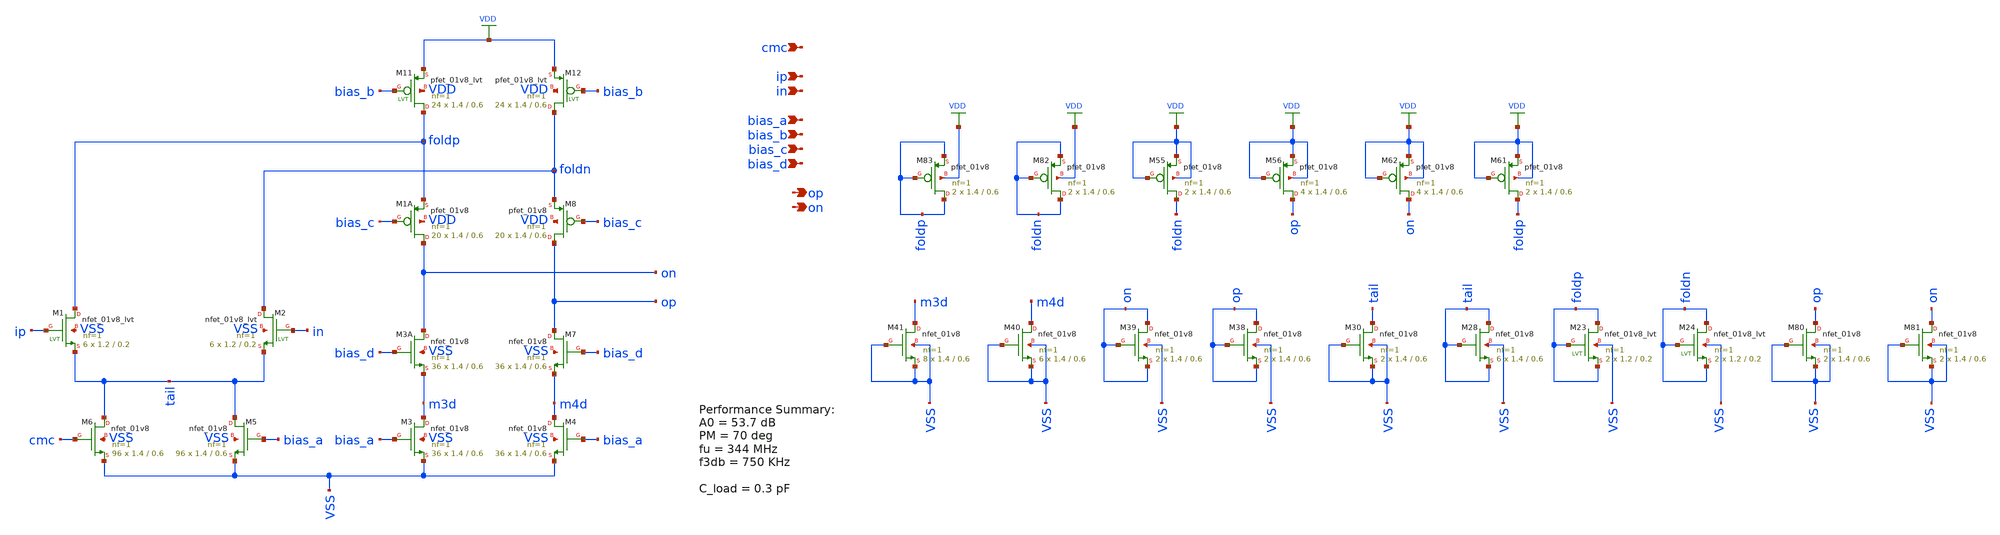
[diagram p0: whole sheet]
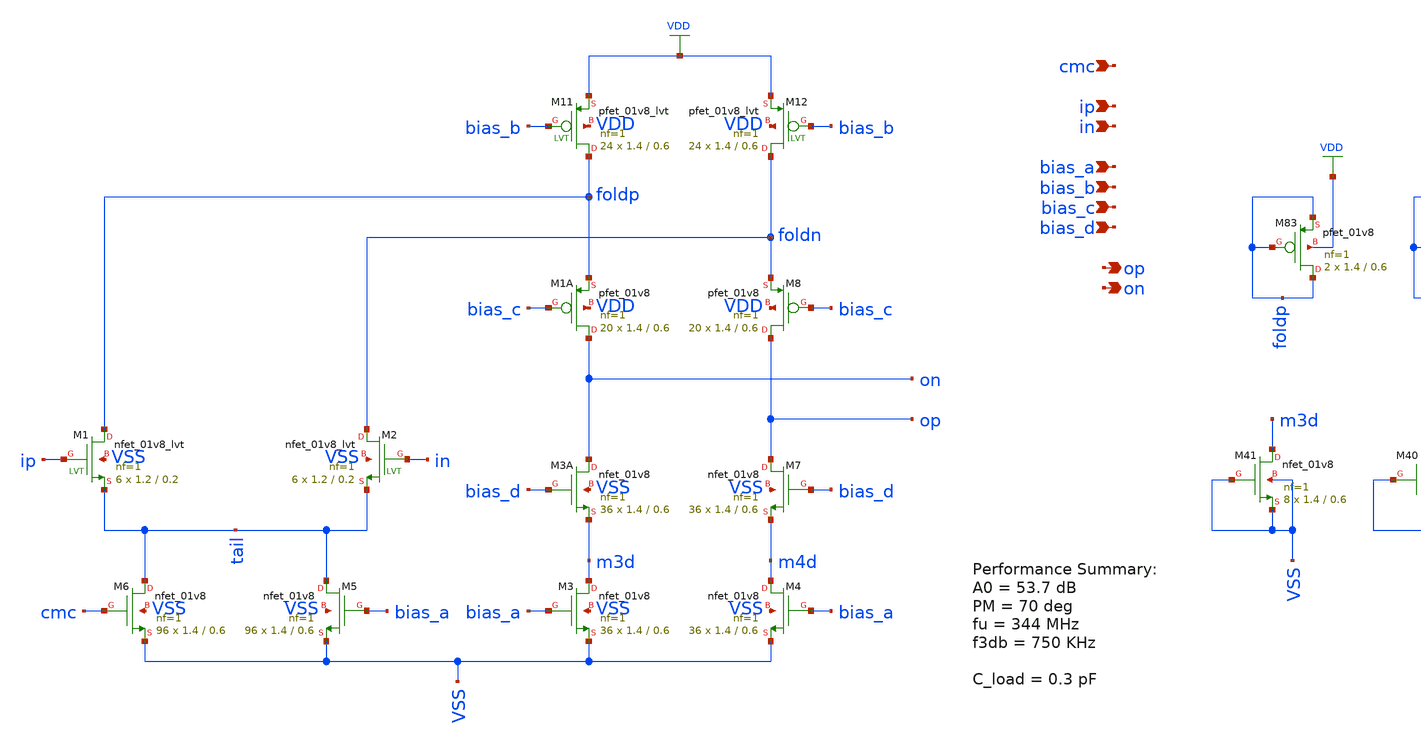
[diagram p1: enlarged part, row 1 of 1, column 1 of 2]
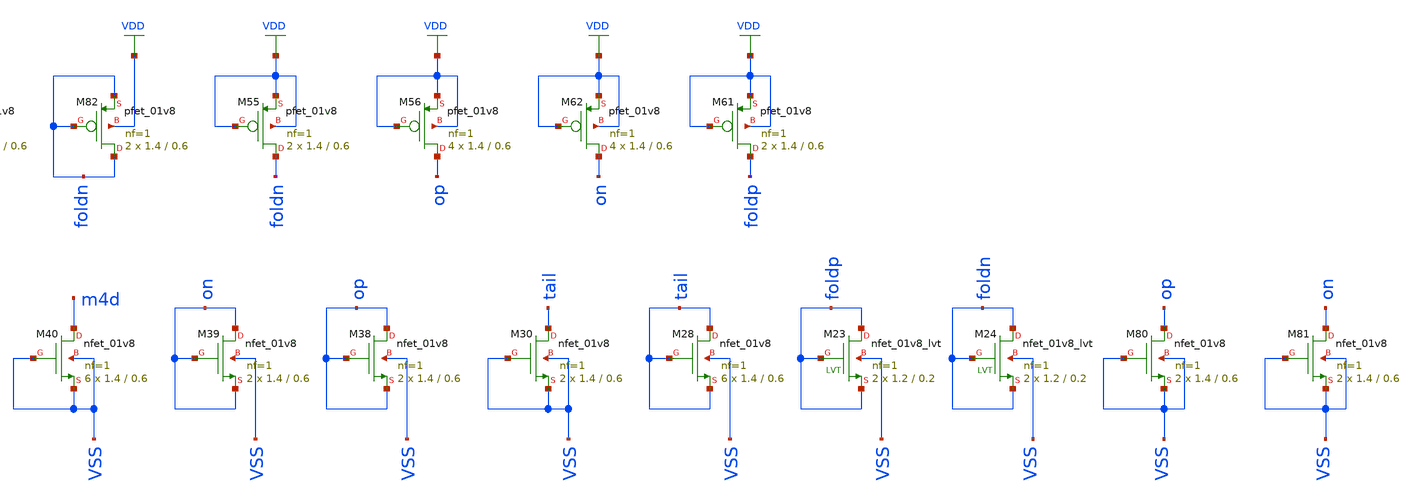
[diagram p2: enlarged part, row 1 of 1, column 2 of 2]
** sch_path: design/analog_modulator/schematic/folded_cascode_3_core.sch
**.subckt folded_cascode_3_core cmc ip in bias_a bias_b bias_c bias_d op on
*.ipin cmc
*.ipin ip
*.ipin in
*.ipin bias_a
*.ipin bias_b
*.ipin bias_c
*.ipin bias_d
*.opin op
*.opin on
XM1 foldp ip tail VSS sky130_fd_pr__nfet_01v8_lvt L=0.2 W=1.2 nf=1 ad='int((nf+1)/2) * W/nf * 0.29' as='int((nf+2)/2) * W/nf * 0.29'
+ pd='2*int((nf+1)/2) * (W/nf + 0.29)' ps='2*int((nf+2)/2) * (W/nf + 0.29)' nrd='0.29 / W' nrs='0.29 / W'
+ sa=0 sb=0 sd=0 mult=6 m=6
XM2 foldn in tail VSS sky130_fd_pr__nfet_01v8_lvt L=0.2 W=1.2 nf=1 ad='int((nf+1)/2) * W/nf * 0.29' as='int((nf+2)/2) * W/nf * 0.29'
+ pd='2*int((nf+1)/2) * (W/nf + 0.29)' ps='2*int((nf+2)/2) * (W/nf + 0.29)' nrd='0.29 / W' nrs='0.29 / W'
+ sa=0 sb=0 sd=0 mult=6 m=6
XM6 tail cmc VSS VSS sky130_fd_pr__nfet_01v8 L=0.6 W=1.4 nf=1 ad='int((nf+1)/2) * W/nf * 0.29' as='int((nf+2)/2) * W/nf * 0.29'
+ pd='2*int((nf+1)/2) * (W/nf + 0.29)' ps='2*int((nf+2)/2) * (W/nf + 0.29)' nrd='0.29 / W' nrs='0.29 / W'
+ sa=0 sb=0 sd=0 mult=96 m=96
XM5 tail bias_a VSS VSS sky130_fd_pr__nfet_01v8 L=0.6 W=1.4 nf=1 ad='int((nf+1)/2) * W/nf * 0.29' as='int((nf+2)/2) * W/nf * 0.29'
+ pd='2*int((nf+1)/2) * (W/nf + 0.29)' ps='2*int((nf+2)/2) * (W/nf + 0.29)' nrd='0.29 / W' nrs='0.29 / W'
+ sa=0 sb=0 sd=0 mult=96 m=96
XM11 foldp bias_b VDD VDD sky130_fd_pr__pfet_01v8_lvt L=0.6 W=1.4 nf=1 ad='int((nf+1)/2) * W/nf * 0.29'
+ as='int((nf+2)/2) * W/nf * 0.29' pd='2*int((nf+1)/2) * (W/nf + 0.29)' ps='2*int((nf+2)/2) * (W/nf + 0.29)'
+ nrd='0.29 / W' nrs='0.29 / W' sa=0 sb=0 sd=0 mult=24 m=24
XM12 foldn bias_b VDD VDD sky130_fd_pr__pfet_01v8_lvt L=0.6 W=1.4 nf=1 ad='int((nf+1)/2) * W/nf * 0.29'
+ as='int((nf+2)/2) * W/nf * 0.29' pd='2*int((nf+1)/2) * (W/nf + 0.29)' ps='2*int((nf+2)/2) * (W/nf + 0.29)'
+ nrd='0.29 / W' nrs='0.29 / W' sa=0 sb=0 sd=0 mult=24 m=24
XM1A on bias_c foldp VDD sky130_fd_pr__pfet_01v8 L=0.6 W=1.4 nf=1 ad='int((nf+1)/2) * W/nf * 0.29' as='int((nf+2)/2) * W/nf * 0.29'
+ pd='2*int((nf+1)/2) * (W/nf + 0.29)' ps='2*int((nf+2)/2) * (W/nf + 0.29)' nrd='0.29 / W' nrs='0.29 / W'
+ sa=0 sb=0 sd=0 mult=20 m=20
XM8 op bias_c foldn VDD sky130_fd_pr__pfet_01v8 L=0.6 W=1.4 nf=1 ad='int((nf+1)/2) * W/nf * 0.29' as='int((nf+2)/2) * W/nf * 0.29'
+ pd='2*int((nf+1)/2) * (W/nf + 0.29)' ps='2*int((nf+2)/2) * (W/nf + 0.29)' nrd='0.29 / W' nrs='0.29 / W'
+ sa=0 sb=0 sd=0 mult=20 m=20
XM3A on bias_d m3d VSS sky130_fd_pr__nfet_01v8 L=0.6 W=1.4 nf=1 ad='int((nf+1)/2) * W/nf * 0.29' as='int((nf+2)/2) * W/nf * 0.29'
+ pd='2*int((nf+1)/2) * (W/nf + 0.29)' ps='2*int((nf+2)/2) * (W/nf + 0.29)' nrd='0.29 / W' nrs='0.29 / W'
+ sa=0 sb=0 sd=0 mult=36 m=36
XM7 op bias_d m4d VSS sky130_fd_pr__nfet_01v8 L=0.6 W=1.4 nf=1 ad='int((nf+1)/2) * W/nf * 0.29' as='int((nf+2)/2) * W/nf * 0.29'
+ pd='2*int((nf+1)/2) * (W/nf + 0.29)' ps='2*int((nf+2)/2) * (W/nf + 0.29)' nrd='0.29 / W' nrs='0.29 / W'
+ sa=0 sb=0 sd=0 mult=36 m=36
XM3 m3d bias_a VSS VSS sky130_fd_pr__nfet_01v8 L=0.6 W=1.4 nf=1 ad='int((nf+1)/2) * W/nf * 0.29' as='int((nf+2)/2) * W/nf * 0.29'
+ pd='2*int((nf+1)/2) * (W/nf + 0.29)' ps='2*int((nf+2)/2) * (W/nf + 0.29)' nrd='0.29 / W' nrs='0.29 / W'
+ sa=0 sb=0 sd=0 mult=36 m=36
XM4 m4d bias_a VSS VSS sky130_fd_pr__nfet_01v8 L=0.6 W=1.4 nf=1 ad='int((nf+1)/2) * W/nf * 0.29' as='int((nf+2)/2) * W/nf * 0.29'
+ pd='2*int((nf+1)/2) * (W/nf + 0.29)' ps='2*int((nf+2)/2) * (W/nf + 0.29)' nrd='0.29 / W' nrs='0.29 / W'
+ sa=0 sb=0 sd=0 mult=36 m=36
XM82 foldn foldn foldn VDD sky130_fd_pr__pfet_01v8 L=0.6 W=1.4 nf=1 ad='int((nf+1)/2) * W/nf * 0.29'
+ as='int((nf+2)/2) * W/nf * 0.29' pd='2*int((nf+1)/2) * (W/nf + 0.29)' ps='2*int((nf+2)/2) * (W/nf + 0.29)'
+ nrd='0.29 / W' nrs='0.29 / W' sa=0 sb=0 sd=0 mult=2 m=2
XM83 foldp foldp foldp VDD sky130_fd_pr__pfet_01v8 L=0.6 W=1.4 nf=1 ad='int((nf+1)/2) * W/nf * 0.29'
+ as='int((nf+2)/2) * W/nf * 0.29' pd='2*int((nf+1)/2) * (W/nf + 0.29)' ps='2*int((nf+2)/2) * (W/nf + 0.29)'
+ nrd='0.29 / W' nrs='0.29 / W' sa=0 sb=0 sd=0 mult=2 m=2
XM55 foldn VDD VDD VDD sky130_fd_pr__pfet_01v8 L=0.6 W=1.4 nf=1 ad='int((nf+1)/2) * W/nf * 0.29' as='int((nf+2)/2) * W/nf * 0.29'
+ pd='2*int((nf+1)/2) * (W/nf + 0.29)' ps='2*int((nf+2)/2) * (W/nf + 0.29)' nrd='0.29 / W' nrs='0.29 / W'
+ sa=0 sb=0 sd=0 mult=2 m=2
XM56 op VDD VDD VDD sky130_fd_pr__pfet_01v8 L=0.6 W=1.4 nf=1 ad='int((nf+1)/2) * W/nf * 0.29' as='int((nf+2)/2) * W/nf * 0.29'
+ pd='2*int((nf+1)/2) * (W/nf + 0.29)' ps='2*int((nf+2)/2) * (W/nf + 0.29)' nrd='0.29 / W' nrs='0.29 / W'
+ sa=0 sb=0 sd=0 mult=4 m=4
XM61 foldp VDD VDD VDD sky130_fd_pr__pfet_01v8 L=0.6 W=1.4 nf=1 ad='int((nf+1)/2) * W/nf * 0.29' as='int((nf+2)/2) * W/nf * 0.29'
+ pd='2*int((nf+1)/2) * (W/nf + 0.29)' ps='2*int((nf+2)/2) * (W/nf + 0.29)' nrd='0.29 / W' nrs='0.29 / W'
+ sa=0 sb=0 sd=0 mult=2 m=2
XM62 on VDD VDD VDD sky130_fd_pr__pfet_01v8 L=0.6 W=1.4 nf=1 ad='int((nf+1)/2) * W/nf * 0.29' as='int((nf+2)/2) * W/nf * 0.29'
+ pd='2*int((nf+1)/2) * (W/nf + 0.29)' ps='2*int((nf+2)/2) * (W/nf + 0.29)' nrd='0.29 / W' nrs='0.29 / W'
+ sa=0 sb=0 sd=0 mult=4 m=4
XM40 m4d VSS VSS VSS sky130_fd_pr__nfet_01v8 L=0.6 W=1.4 nf=1 ad='int((nf+1)/2) * W/nf * 0.29' as='int((nf+2)/2) * W/nf * 0.29'
+ pd='2*int((nf+1)/2) * (W/nf + 0.29)' ps='2*int((nf+2)/2) * (W/nf + 0.29)' nrd='0.29 / W' nrs='0.29 / W'
+ sa=0 sb=0 sd=0 mult=6 m=6
XM41 m3d VSS VSS VSS sky130_fd_pr__nfet_01v8 L=0.6 W=1.4 nf=1 ad='int((nf+1)/2) * W/nf * 0.29' as='int((nf+2)/2) * W/nf * 0.29'
+ pd='2*int((nf+1)/2) * (W/nf + 0.29)' ps='2*int((nf+2)/2) * (W/nf + 0.29)' nrd='0.29 / W' nrs='0.29 / W'
+ sa=0 sb=0 sd=0 mult=8 m=8
XM38 op op op VSS sky130_fd_pr__nfet_01v8 L=0.6 W=1.4 nf=1 ad='int((nf+1)/2) * W/nf * 0.29' as='int((nf+2)/2) * W/nf * 0.29'
+ pd='2*int((nf+1)/2) * (W/nf + 0.29)' ps='2*int((nf+2)/2) * (W/nf + 0.29)' nrd='0.29 / W' nrs='0.29 / W'
+ sa=0 sb=0 sd=0 mult=2 m=2
XM39 on on on VSS sky130_fd_pr__nfet_01v8 L=0.6 W=1.4 nf=1 ad='int((nf+1)/2) * W/nf * 0.29' as='int((nf+2)/2) * W/nf * 0.29'
+ pd='2*int((nf+1)/2) * (W/nf + 0.29)' ps='2*int((nf+2)/2) * (W/nf + 0.29)' nrd='0.29 / W' nrs='0.29 / W'
+ sa=0 sb=0 sd=0 mult=2 m=2
XM30 tail VSS VSS VSS sky130_fd_pr__nfet_01v8 L=0.6 W=1.4 nf=1 ad='int((nf+1)/2) * W/nf * 0.29' as='int((nf+2)/2) * W/nf * 0.29'
+ pd='2*int((nf+1)/2) * (W/nf + 0.29)' ps='2*int((nf+2)/2) * (W/nf + 0.29)' nrd='0.29 / W' nrs='0.29 / W'
+ sa=0 sb=0 sd=0 mult=2 m=2
XM23 foldp foldp foldp VSS sky130_fd_pr__nfet_01v8_lvt L=0.2 W=1.2 nf=1 ad='int((nf+1)/2) * W/nf * 0.29'
+ as='int((nf+2)/2) * W/nf * 0.29' pd='2*int((nf+1)/2) * (W/nf + 0.29)' ps='2*int((nf+2)/2) * (W/nf + 0.29)'
+ nrd='0.29 / W' nrs='0.29 / W' sa=0 sb=0 sd=0 mult=2 m=2
XM24 foldn foldn foldn VSS sky130_fd_pr__nfet_01v8_lvt L=0.2 W=1.2 nf=1 ad='int((nf+1)/2) * W/nf * 0.29'
+ as='int((nf+2)/2) * W/nf * 0.29' pd='2*int((nf+1)/2) * (W/nf + 0.29)' ps='2*int((nf+2)/2) * (W/nf + 0.29)'
+ nrd='0.29 / W' nrs='0.29 / W' sa=0 sb=0 sd=0 mult=2 m=2
XM80 op VSS VSS VSS sky130_fd_pr__nfet_01v8 L=0.6 W=1.4 nf=1 ad='int((nf+1)/2) * W/nf * 0.29' as='int((nf+2)/2) * W/nf * 0.29'
+ pd='2*int((nf+1)/2) * (W/nf + 0.29)' ps='2*int((nf+2)/2) * (W/nf + 0.29)' nrd='0.29 / W' nrs='0.29 / W'
+ sa=0 sb=0 sd=0 mult=2 m=2
XM81 on VSS VSS VSS sky130_fd_pr__nfet_01v8 L=0.6 W=1.4 nf=1 ad='int((nf+1)/2) * W/nf * 0.29' as='int((nf+2)/2) * W/nf * 0.29'
+ pd='2*int((nf+1)/2) * (W/nf + 0.29)' ps='2*int((nf+2)/2) * (W/nf + 0.29)' nrd='0.29 / W' nrs='0.29 / W'
+ sa=0 sb=0 sd=0 mult=2 m=2
XM28 tail tail tail VSS sky130_fd_pr__nfet_01v8 L=0.6 W=1.4 nf=1 ad='int((nf+1)/2) * W/nf * 0.29' as='int((nf+2)/2) * W/nf * 0.29'
+ pd='2*int((nf+1)/2) * (W/nf + 0.29)' ps='2*int((nf+2)/2) * (W/nf + 0.29)' nrd='0.29 / W' nrs='0.29 / W'
+ sa=0 sb=0 sd=0 mult=6 m=6
**.ends
.GLOBAL VDD
.end
